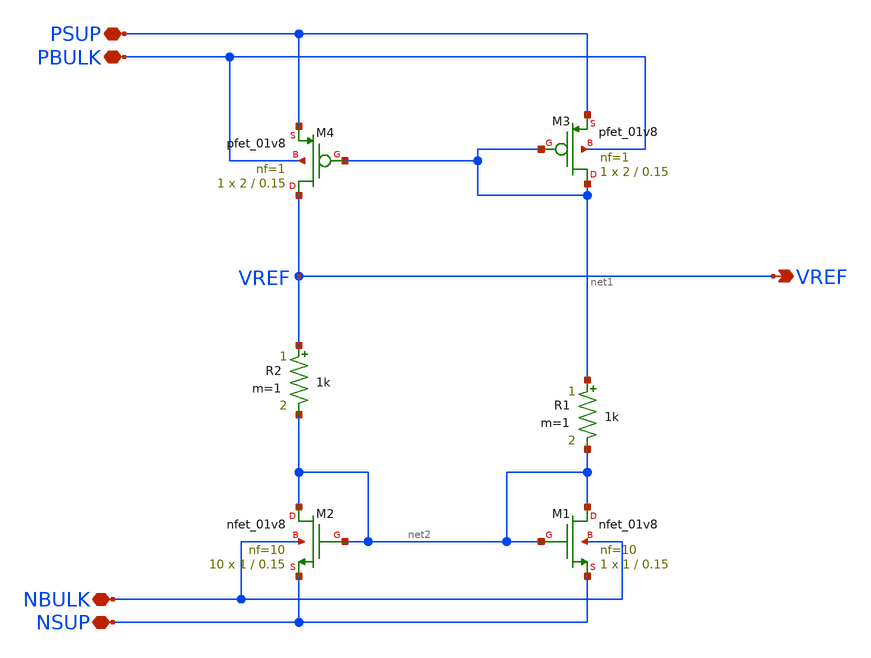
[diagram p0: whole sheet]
** sch_path: xschem/Bandgap.sch
**.subckt Bandgap PSUP NSUP NBULK VREF PBULK
*.iopin PSUP
*.iopin NSUP
*.iopin NBULK
*.opin VREF
*.iopin PBULK
XM1 net2 net2 NSUP NBULK sky130_fd_pr__nfet_01v8 L=0.15 W=1 nf=10 ad='int((10 + 1)/2) * 1 / 10 * 0.29'
+ as='int((10 + 2)/2) * 1 / 10 * 0.29' pd='2*int((10 + 1)/2) * (1 / 10 + 0.29)' ps='2*int((10 + 2)/2) * (1 / 10 + 0.29)'
+ nrd='0.29 / 1 ' nrs='0.29 / 1 ' sa=0 sb=0 sd=0 mult=1 m=1
XM2 net2 net2 NSUP NBULK sky130_fd_pr__nfet_01v8 L=0.15 W=1 nf=10 ad='int((10 + 1)/2) * 1 / 10 * 0.29'
+ as='int((10 + 2)/2) * 1 / 10 * 0.29' pd='2*int((10 + 1)/2) * (1 / 10 + 0.29)' ps='2*int((10 + 2)/2) * (1 / 10 + 0.29)'
+ nrd='0.29 / 1 ' nrs='0.29 / 1 ' sa=0 sb=0 sd=0 mult=10 m=10
R1 net1 net2 1k m=1
R2 VREF net2 1k m=1
XM3 net1 net1 PSUP PBULK sky130_fd_pr__pfet_01v8 L=0.15 W=2 nf=1 ad='int((nf+1)/2) * W/nf * 0.29' as='int((nf+2)/2) * W/nf * 0.29'
+ pd='2*int((nf+1)/2) * (W/nf + 0.29)' ps='2*int((nf+2)/2) * (W/nf + 0.29)' nrd='0.29 / W' nrs='0.29 / W'
+ sa=0 sb=0 sd=0 mult=1 m=1
XM4 VREF net1 PSUP PBULK sky130_fd_pr__pfet_01v8 L=0.15 W=2 nf=1 ad='int((nf+1)/2) * W/nf * 0.29' as='int((nf+2)/2) * W/nf * 0.29'
+ pd='2*int((nf+1)/2) * (W/nf + 0.29)' ps='2*int((nf+2)/2) * (W/nf + 0.29)' nrd='0.29 / W' nrs='0.29 / W'
+ sa=0 sb=0 sd=0 mult=1 m=1
**.ends
.end
